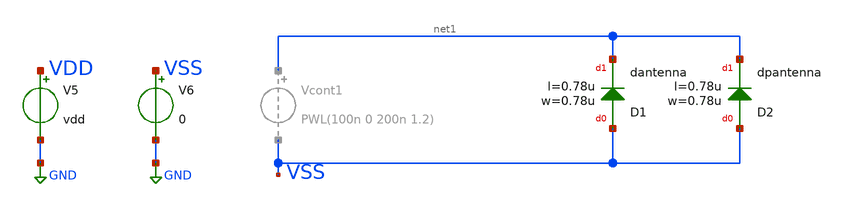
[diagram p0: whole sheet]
** sch_path: QDLL6501-main/schematic/xschem/testbenches/untitled-1.sch
**.subckt untitled-1
V5 VDD GND vdd
V6 VSS GND 0
XD1 VSS net1 dantenna l=0.78u w=0.78u
XD2 VSS net1 dpantenna l=0.78u w=0.78u
**** begin user architecture code


.param temp=65 vdd=1.2
.param per=4n duty=2n tr=20p tf=20p delay=2n
.param vin=1.2 vd={vdd}


.lib cornerMOSlv.lib mos_tt
.lib cornerCAP.lib cap_typ
.lib cornerRES.lib res_typ

.endc


**** end user architecture code
**.ends
.GLOBAL GND
.end
